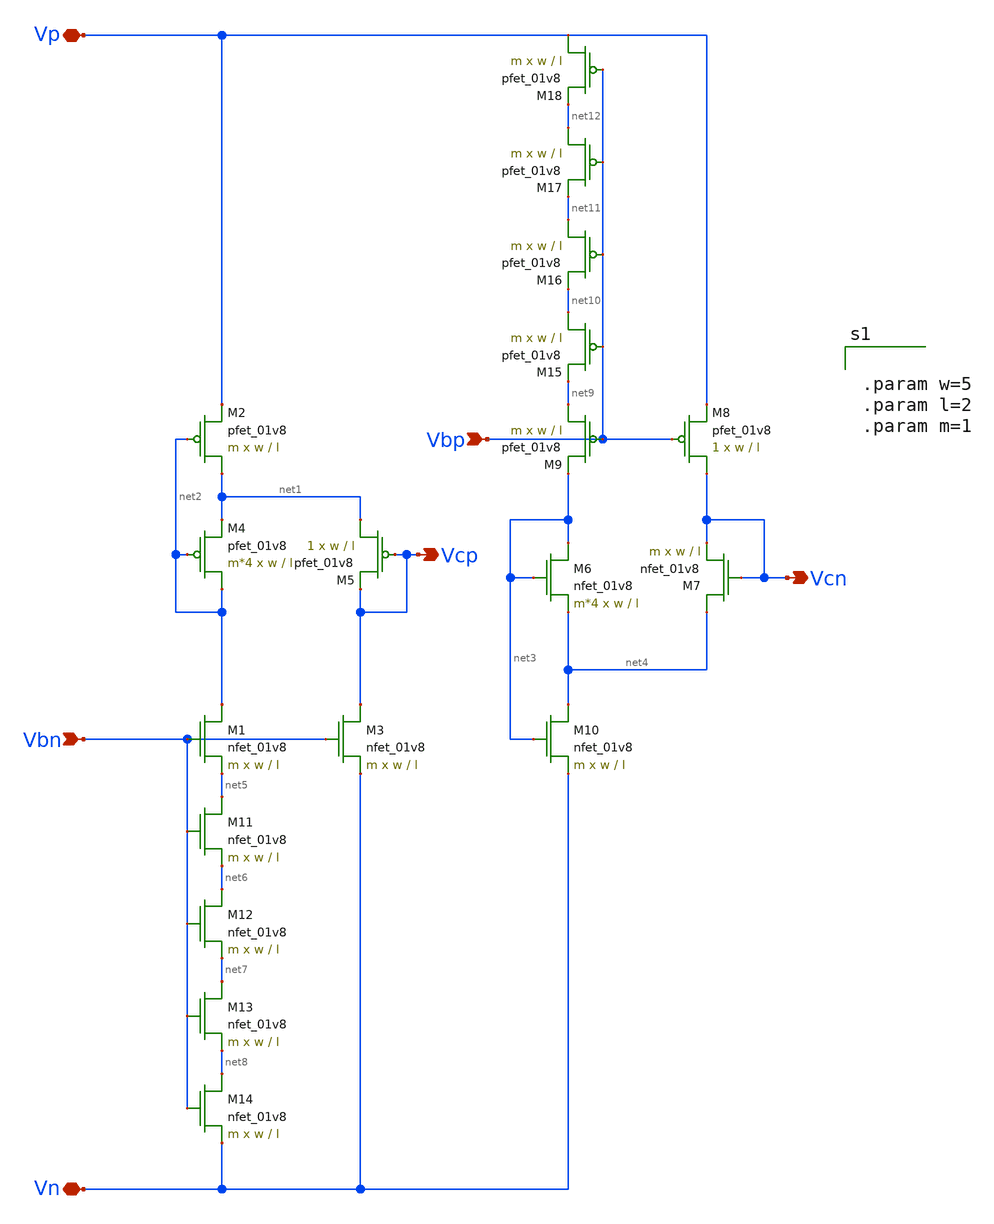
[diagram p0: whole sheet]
** sch_path: schematic/cascode_generator.sch
**.subckt cascode_generator Vbp Vbn Vn Vp Vcp Vcn
*.ipin Vbp
*.ipin Vbn
*.iopin Vn
*.iopin Vp
*.opin Vcp
*.opin Vcn
XM1 net2 Vbn net5 GND sky130_fd_pr__nfet_01v8 L=l W=w nf=1 ad='int((nf+1)/2) * W/nf * 0.29' as='int((nf+2)/2) * W/nf * 0.29'
+ pd='2*int((nf+1)/2) * (W/nf + 0.29)' ps='2*int((nf+2)/2) * (W/nf + 0.29)' nrd='0.29 / W' nrs='0.29 / W'
+ sa=0 sb=0 sd=0 mult=m m=m
XM2 net1 net2 Vp VDD sky130_fd_pr__pfet_01v8 L=l W=w nf=1 ad='int((nf+1)/2) * W/nf * 0.29' as='int((nf+2)/2) * W/nf * 0.29'
+ pd='2*int((nf+1)/2) * (W/nf + 0.29)' ps='2*int((nf+2)/2) * (W/nf + 0.29)' nrd='0.29 / W' nrs='0.29 / W'
+ sa=0 sb=0 sd=0 mult=m m=m
XM3 Vcp Vbn Vn GND sky130_fd_pr__nfet_01v8 L=l W=w nf=1 ad='int((nf+1)/2) * W/nf * 0.29' as='int((nf+2)/2) * W/nf * 0.29'
+ pd='2*int((nf+1)/2) * (W/nf + 0.29)' ps='2*int((nf+2)/2) * (W/nf + 0.29)' nrd='0.29 / W' nrs='0.29 / W'
+ sa=0 sb=0 sd=0 mult=m m=m
XM4 net2 net2 net1 VDD sky130_fd_pr__pfet_01v8 L=l W=w nf=1 ad='int((nf+1)/2) * W/nf * 0.29' as='int((nf+2)/2) * W/nf * 0.29'
+ pd='2*int((nf+1)/2) * (W/nf + 0.29)' ps='2*int((nf+2)/2) * (W/nf + 0.29)' nrd='0.29 / W' nrs='0.29 / W'
+ sa=0 sb=0 sd=0 mult=m*4 m=m*4
XM5 net1 Vcp Vcp VDD sky130_fd_pr__pfet_01v8 L=l W=w nf=1 ad='int((nf+1)/2) * W/nf * 0.29' as='int((nf+2)/2) * W/nf * 0.29'
+ pd='2*int((nf+1)/2) * (W/nf + 0.29)' ps='2*int((nf+2)/2) * (W/nf + 0.29)' nrd='0.29 / W' nrs='0.29 / W'
+ sa=0 sb=0 sd=0 mult=1 m=1
XM6 net3 net3 net4 GND sky130_fd_pr__nfet_01v8 L=l W=w nf=1 ad='int((nf+1)/2) * W/nf * 0.29' as='int((nf+2)/2) * W/nf * 0.29'
+ pd='2*int((nf+1)/2) * (W/nf + 0.29)' ps='2*int((nf+2)/2) * (W/nf + 0.29)' nrd='0.29 / W' nrs='0.29 / W'
+ sa=0 sb=0 sd=0 mult=m*4 m=m*4
XM7 net4 Vcn Vcn GND sky130_fd_pr__nfet_01v8 L=l W=w nf=1 ad='int((nf+1)/2) * W/nf * 0.29' as='int((nf+2)/2) * W/nf * 0.29'
+ pd='2*int((nf+1)/2) * (W/nf + 0.29)' ps='2*int((nf+2)/2) * (W/nf + 0.29)' nrd='0.29 / W' nrs='0.29 / W'
+ sa=0 sb=0 sd=0 mult=m m=m
XM8 Vcn Vbp Vp VDD sky130_fd_pr__pfet_01v8 L=l W=w nf=1 ad='int((nf+1)/2) * W/nf * 0.29' as='int((nf+2)/2) * W/nf * 0.29'
+ pd='2*int((nf+1)/2) * (W/nf + 0.29)' ps='2*int((nf+2)/2) * (W/nf + 0.29)' nrd='0.29 / W' nrs='0.29 / W'
+ sa=0 sb=0 sd=0 mult=1 m=1
XM9 net9 Vbp net3 VDD sky130_fd_pr__pfet_01v8 L=l W=w nf=1 ad='int((nf+1)/2) * W/nf * 0.29' as='int((nf+2)/2) * W/nf * 0.29'
+ pd='2*int((nf+1)/2) * (W/nf + 0.29)' ps='2*int((nf+2)/2) * (W/nf + 0.29)' nrd='0.29 / W' nrs='0.29 / W'
+ sa=0 sb=0 sd=0 mult=m m=m
XM10 net4 net3 Vn GND sky130_fd_pr__nfet_01v8 L=l W=w nf=1 ad='int((nf+1)/2) * W/nf * 0.29' as='int((nf+2)/2) * W/nf * 0.29'
+ pd='2*int((nf+1)/2) * (W/nf + 0.29)' ps='2*int((nf+2)/2) * (W/nf + 0.29)' nrd='0.29 / W' nrs='0.29 / W'
+ sa=0 sb=0 sd=0 mult=m m=m
XM11 net5 Vbn net6 GND sky130_fd_pr__nfet_01v8 L=l W=w nf=1 ad='int((nf+1)/2) * W/nf * 0.29' as='int((nf+2)/2) * W/nf * 0.29'
+ pd='2*int((nf+1)/2) * (W/nf + 0.29)' ps='2*int((nf+2)/2) * (W/nf + 0.29)' nrd='0.29 / W' nrs='0.29 / W'
+ sa=0 sb=0 sd=0 mult=m m=m
XM12 net6 Vbn net7 GND sky130_fd_pr__nfet_01v8 L=l W=w nf=1 ad='int((nf+1)/2) * W/nf * 0.29' as='int((nf+2)/2) * W/nf * 0.29'
+ pd='2*int((nf+1)/2) * (W/nf + 0.29)' ps='2*int((nf+2)/2) * (W/nf + 0.29)' nrd='0.29 / W' nrs='0.29 / W'
+ sa=0 sb=0 sd=0 mult=m m=m
XM13 net7 Vbn net8 GND sky130_fd_pr__nfet_01v8 L=l W=w nf=1 ad='int((nf+1)/2) * W/nf * 0.29' as='int((nf+2)/2) * W/nf * 0.29'
+ pd='2*int((nf+1)/2) * (W/nf + 0.29)' ps='2*int((nf+2)/2) * (W/nf + 0.29)' nrd='0.29 / W' nrs='0.29 / W'
+ sa=0 sb=0 sd=0 mult=m m=m
XM14 net8 Vbn Vn GND sky130_fd_pr__nfet_01v8 L=l W=w nf=1 ad='int((nf+1)/2) * W/nf * 0.29' as='int((nf+2)/2) * W/nf * 0.29'
+ pd='2*int((nf+1)/2) * (W/nf + 0.29)' ps='2*int((nf+2)/2) * (W/nf + 0.29)' nrd='0.29 / W' nrs='0.29 / W'
+ sa=0 sb=0 sd=0 mult=m m=m
XM15 net10 Vbp net9 VDD sky130_fd_pr__pfet_01v8 L=l W=w nf=1 ad='int((nf+1)/2) * W/nf * 0.29' as='int((nf+2)/2) * W/nf * 0.29'
+ pd='2*int((nf+1)/2) * (W/nf + 0.29)' ps='2*int((nf+2)/2) * (W/nf + 0.29)' nrd='0.29 / W' nrs='0.29 / W'
+ sa=0 sb=0 sd=0 mult=m m=m
XM16 net11 Vbp net10 VDD sky130_fd_pr__pfet_01v8 L=l W=w nf=1 ad='int((nf+1)/2) * W/nf * 0.29' as='int((nf+2)/2) * W/nf * 0.29'
+ pd='2*int((nf+1)/2) * (W/nf + 0.29)' ps='2*int((nf+2)/2) * (W/nf + 0.29)' nrd='0.29 / W' nrs='0.29 / W'
+ sa=0 sb=0 sd=0 mult=m m=m
XM17 net12 Vbp net11 VDD sky130_fd_pr__pfet_01v8 L=l W=w nf=1 ad='int((nf+1)/2) * W/nf * 0.29' as='int((nf+2)/2) * W/nf * 0.29'
+ pd='2*int((nf+1)/2) * (W/nf + 0.29)' ps='2*int((nf+2)/2) * (W/nf + 0.29)' nrd='0.29 / W' nrs='0.29 / W'
+ sa=0 sb=0 sd=0 mult=m m=m
XM18 Vp Vbp net12 VDD sky130_fd_pr__pfet_01v8 L=l W=w nf=1 ad='int((nf+1)/2) * W/nf * 0.29' as='int((nf+2)/2) * W/nf * 0.29'
+ pd='2*int((nf+1)/2) * (W/nf + 0.29)' ps='2*int((nf+2)/2) * (W/nf + 0.29)' nrd='0.29 / W' nrs='0.29 / W'
+ sa=0 sb=0 sd=0 mult=m m=m
**** begin user architecture code


.param w=5
.param l=2
.param m=1


**** end user architecture code
**.ends
.end
